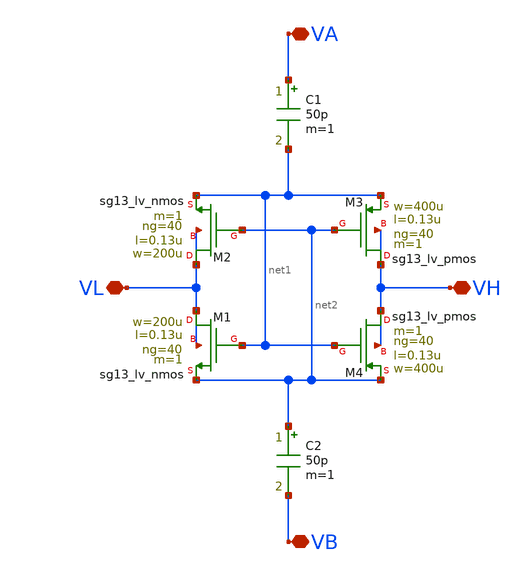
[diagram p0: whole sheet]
** sch_path: analog/core/rect_01_10k.sch
**.subckt rect_01_10k VL VH VA VB
*.iopin VL
*.iopin VH
*.iopin VA
*.iopin VB
XM1 VL net1 net2 VL sg13_lv_nmos w=200u l=0.13u ng=40 m=1 mm_ok=1
XM3 VH net2 net1 VH sg13_lv_pmos w=400u l=0.13u ng=40 m=1 mm_ok=1
XM2 VL net2 net1 VL sg13_lv_nmos w=200u l=0.13u ng=40 m=1 mm_ok=1
XM4 VH net1 net2 VH sg13_lv_pmos w=400u l=0.13u ng=40 m=1 mm_ok=1
C1 VA net1 50p m=1
C2 net2 VB 50p m=1
**.ends
.end
